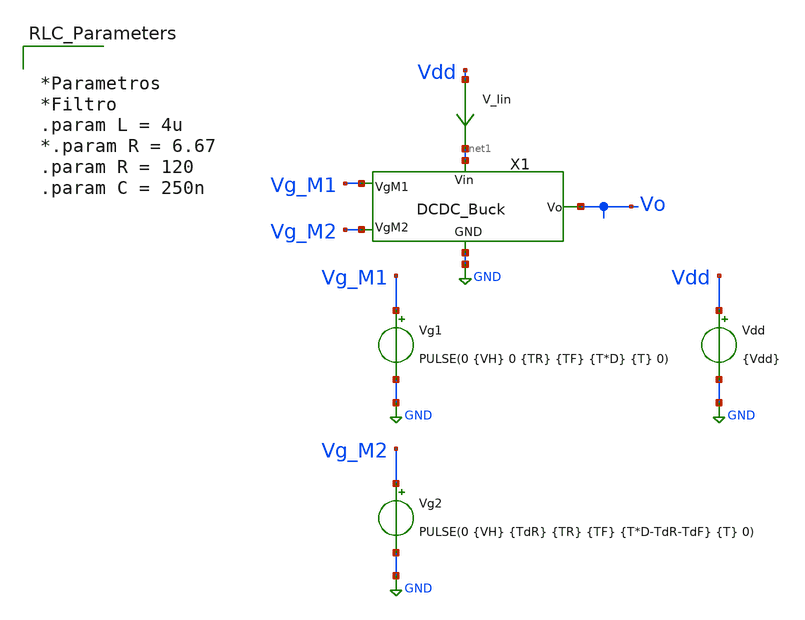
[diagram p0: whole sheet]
** sch_path: xschem/TB_DCDCBuck_SKY130.sch
.lib $::SKYWATER_MODELS/sky130.lib.spice tt
.include $::SKYWATER_STDCELLS/sky130_fd_sc_hd.spice

**.subckt TB_DCDCBuck_SKY130
Vdd Vdd GND {Vdd}
Vg2 Vg_M2 GND PULSE(0 {VH} {TdR} {TR} {TF} {T*D-TdR-TdF} {T} 0)
Vg1 Vg_M1 GND PULSE(0 {VH} 0 {TR} {TF} {T*D} {T} 0)
V_Iin Vdd net1 0
.save i(v_iin)
X1 Vg_M1 Vg_M2 GND net1 Vo DCDC_Buck
**** begin user architecture code


.param temp=27
.param mult_M1 = 2400
.param w_M1 =10u
*.param l_M1 = 0.2u ** Posee mayor capacidad de corriente, pero en sub-umbral conduce mucha
*+ corriente
.param l_M1 = 0.22u
.param ng_M1 = 1

.param mult_M2 = 1200
.param w_M2 =10u
.param l_M2 =0.25u
.param ng_M2 =1







.param Vdd = 3.3
.param VH = 3.3
.param Del = 0

.param D = 0.416
.param T = 0.5u
.param TR = 13.5n
.param TF = 13.5n
.param TdR = 5n
.param TdF = 5n


.param temp = 27





.save all  @m.x1.xm1.msky130_fd_pr__pfet_g5v0d10v5[id]  @m.x1.xm2.msky130_fd_pr__nfet_g5v0d10v5[id]
.param SimTime = 5u

.control
reset
set color0 = white
tran 1n 30u
let Io = i(v.x1.V_Io)
let Id_M1 = @m.x1.xm1.msky130_fd_pr__pfet_g5v0d10v5[id]
let Id_M2 = @m.x1.xm2.msky130_fd_pr__nfet_g5v0d10v5[id]
let Po = Io*v(Vo)
let I_in = i(V_Iin)
let Pin = I_in*v(Vdd)
let Vsd_M1 = v(Vdd) - v(x1.Vc)
let Vds_M2 = v(x1.Vc)
let P_M1 = Vsd_M1*Id_M1
let P_M2 = -Vds_M2*Id_M2
let DataMeasBegin = SimTime-1u

meas tran Vo_mean AVG v(Vo) from=20u to=30u
meas tran Io_mean AVG Io from=20u to=30u
meas tran Po_mean AVG Po from=20u to=30u
meas tran Pin_mean AVG Pin from=20u to=30u
meas tran P_M1_mean AVG P_M1 from=20u to=30u
meas tran P_M2_mean AVG P_M2 from=20u to=30u

let eff = 100*Po_mean/Pin_mean
let loss_M1 = 100*P_M1_mean/Pin_mean
let loss_M2 = 100*P_M2_mean/Pin_mean
let sumaPot = eff+loss_M1+loss_M2
print eff loss_M1 loss_M2 sumaPot

plot Io i(v.x1.V_IL)
plot Id_M1 Id_M2
plot v(Vo)
plot Po Pin
*plot P_M1 P_M2
plot v(x1.Vc)
plot v(Vg_M1) v(Vg_M2)
.endc



.end




*Parametros
*Filtro
.param L = 4u
*.param R = 6.67
.param R = 120
.param C = 250n




**** end user architecture code
**.ends

* expanding   symbol:  /home/designer/shared/TO202406_CMOSVCO_Esm22/xschem/Modulos/DCDC_Buck.sym #
*+ of pins=5
** sym_path: /home/designer/shared/TO202406_CMOSVCO_Esm22/xschem/Modulos/DCDC_Buck.sym
** sch_path: /home/designer/shared/TO202406_CMOSVCO_Esm22/xschem/Modulos/DCDC_Buck.sch
.subckt DCDC_Buck VgM1 VgM2 GND Vin Vo
*.iopin Vin
*.ipin VgM1
*.ipin VgM2
*.iopin Vo
*.iopin GND
L1 net2 net1 {L} m=1
C1 net1 GND {C} m=1
V_Io net1 Vo 0
.save i(v_io)
V_IL Vc net2 0
.save i(v_il)
R1 Vo GND {R} m=1
XM1 Vc VgM1 Vin Vin sky130_fd_pr__pfet_g5v0d10v5 L=0.5 W=4.38 nf=1 ad='int((nf+1)/2) * W/nf * 0.29' as='int((nf+2)/2) * W/nf * 0.29'
+ pd='2*int((nf+1)/2) * (W/nf + 0.29)' ps='2*int((nf+2)/2) * (W/nf + 0.29)' nrd='0.29 / W' nrs='0.29 / W'
+ sa=0 sb=0 sd=0 mult=4506 m=4506
XM2 Vc VgM2 GND GND sky130_fd_pr__nfet_g5v0d10v5 L=0.5 W=4.38 nf=1 ad='int((nf+1)/2) * W/nf * 0.29' as='int((nf+2)/2) * W/nf * 0.29'
+ pd='2*int((nf+1)/2) * (W/nf + 0.29)' ps='2*int((nf+2)/2) * (W/nf + 0.29)' nrd='0.29 / W' nrs='0.29 / W'
+ sa=0 sb=0 sd=0 mult=2520 m=2520
.ends

.GLOBAL GND
.end
